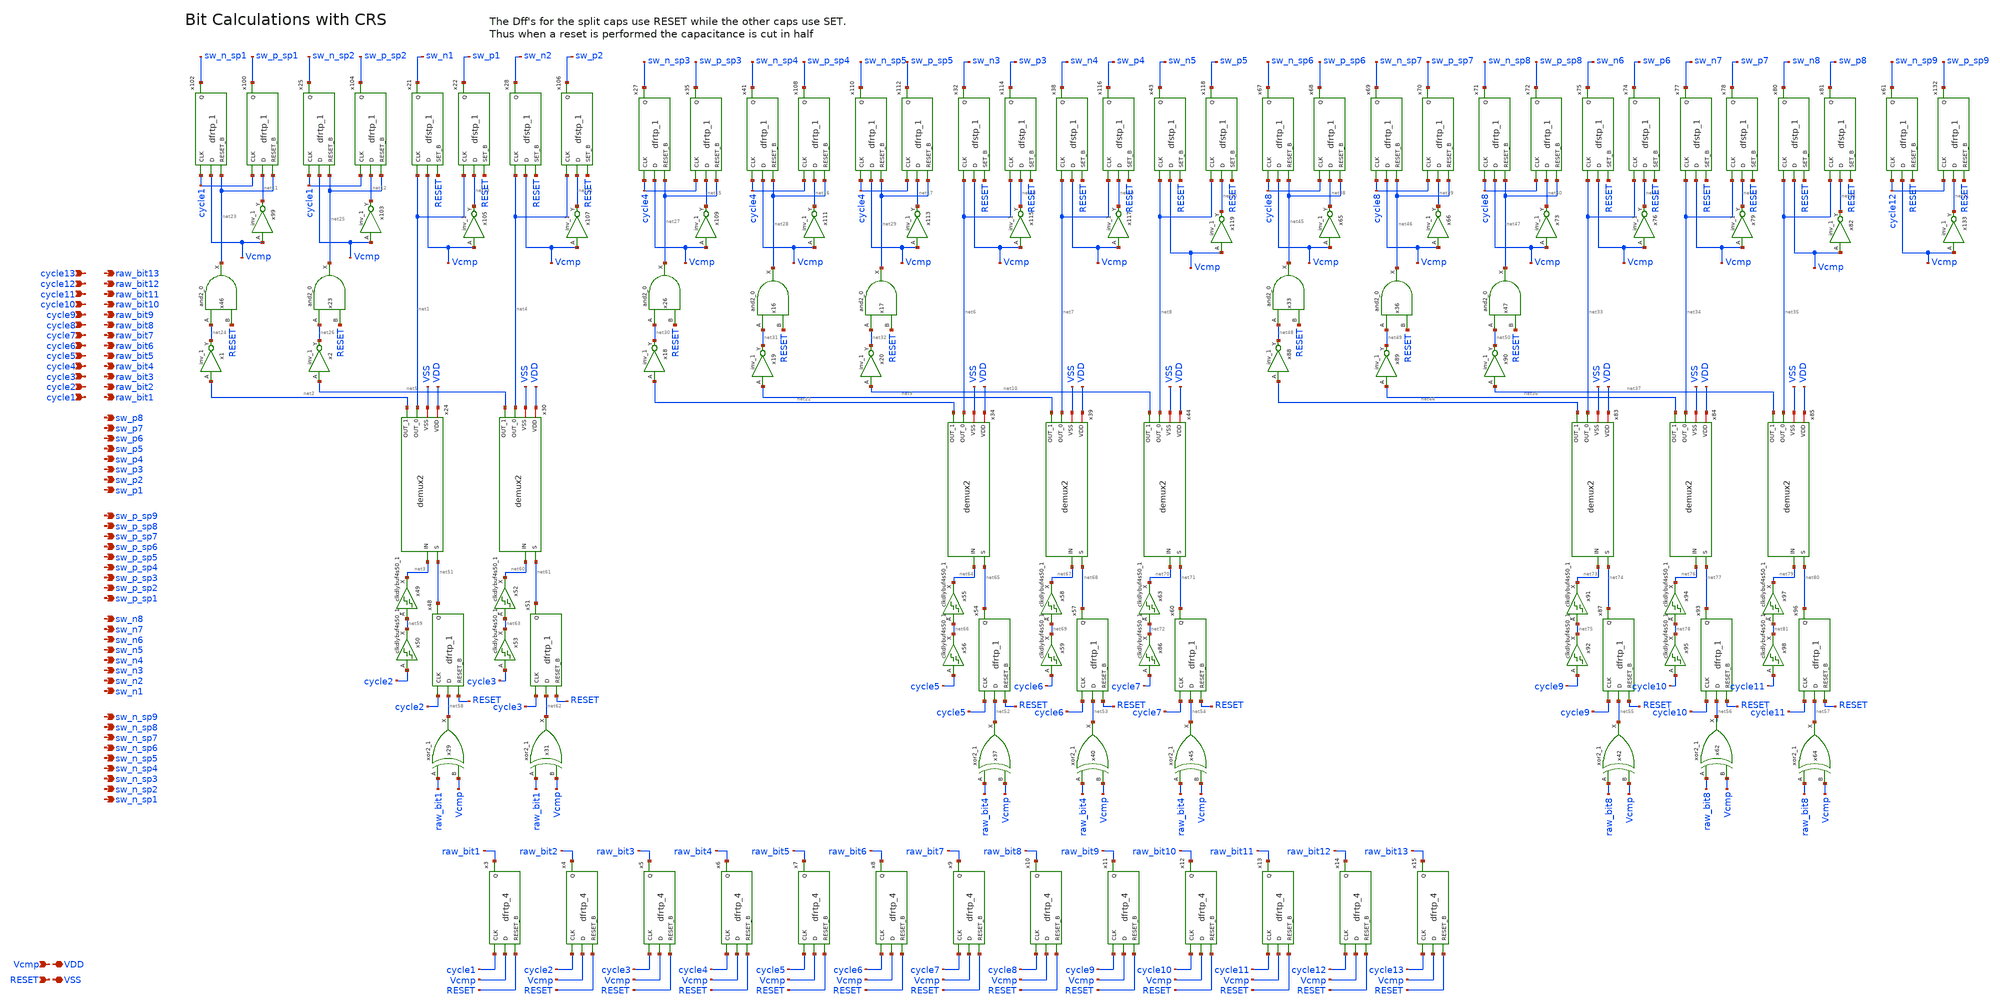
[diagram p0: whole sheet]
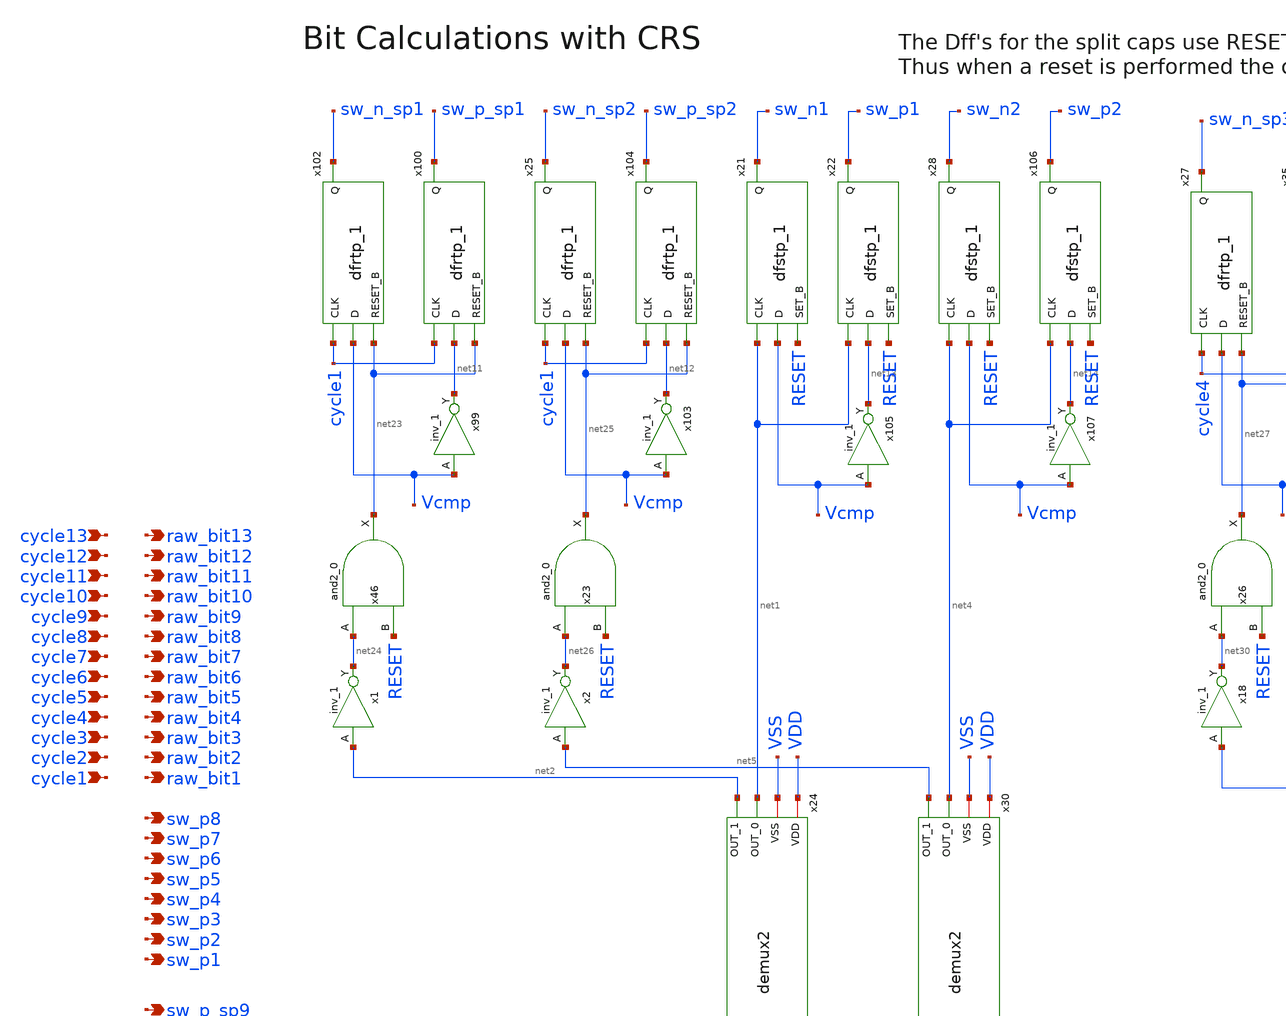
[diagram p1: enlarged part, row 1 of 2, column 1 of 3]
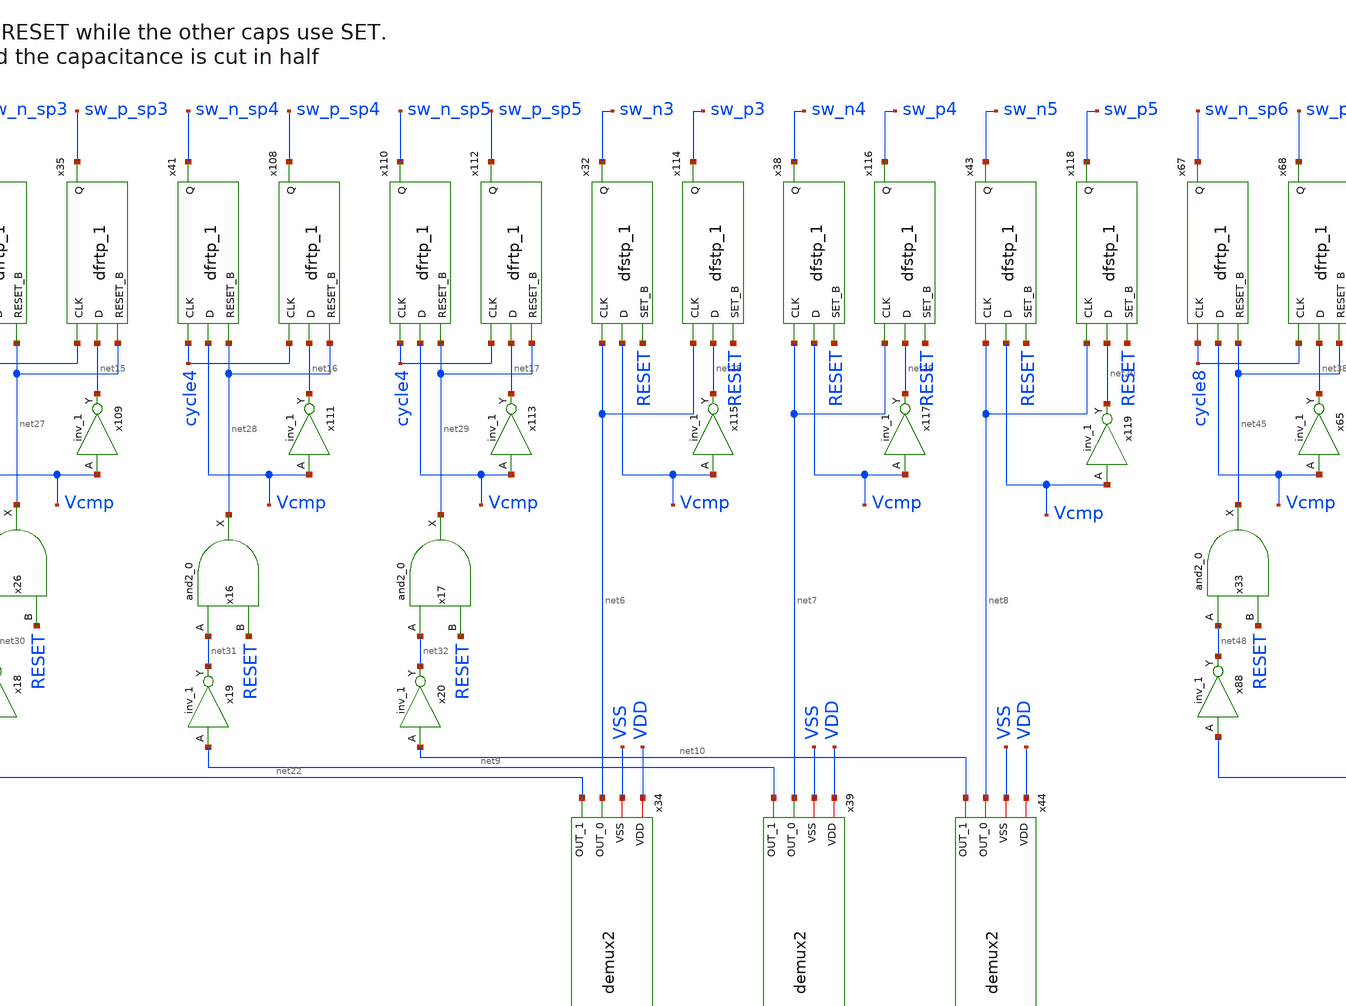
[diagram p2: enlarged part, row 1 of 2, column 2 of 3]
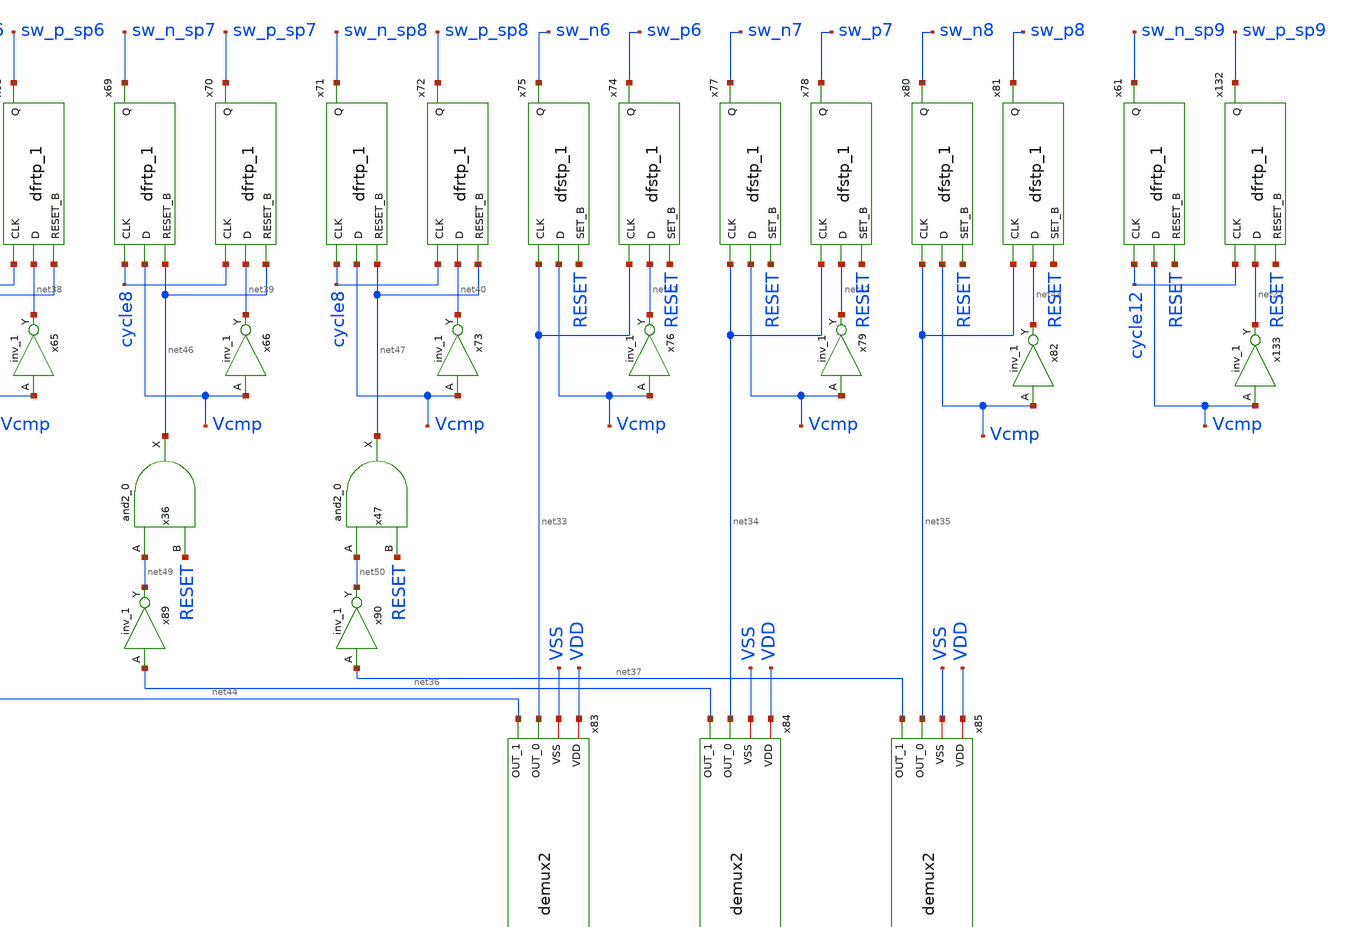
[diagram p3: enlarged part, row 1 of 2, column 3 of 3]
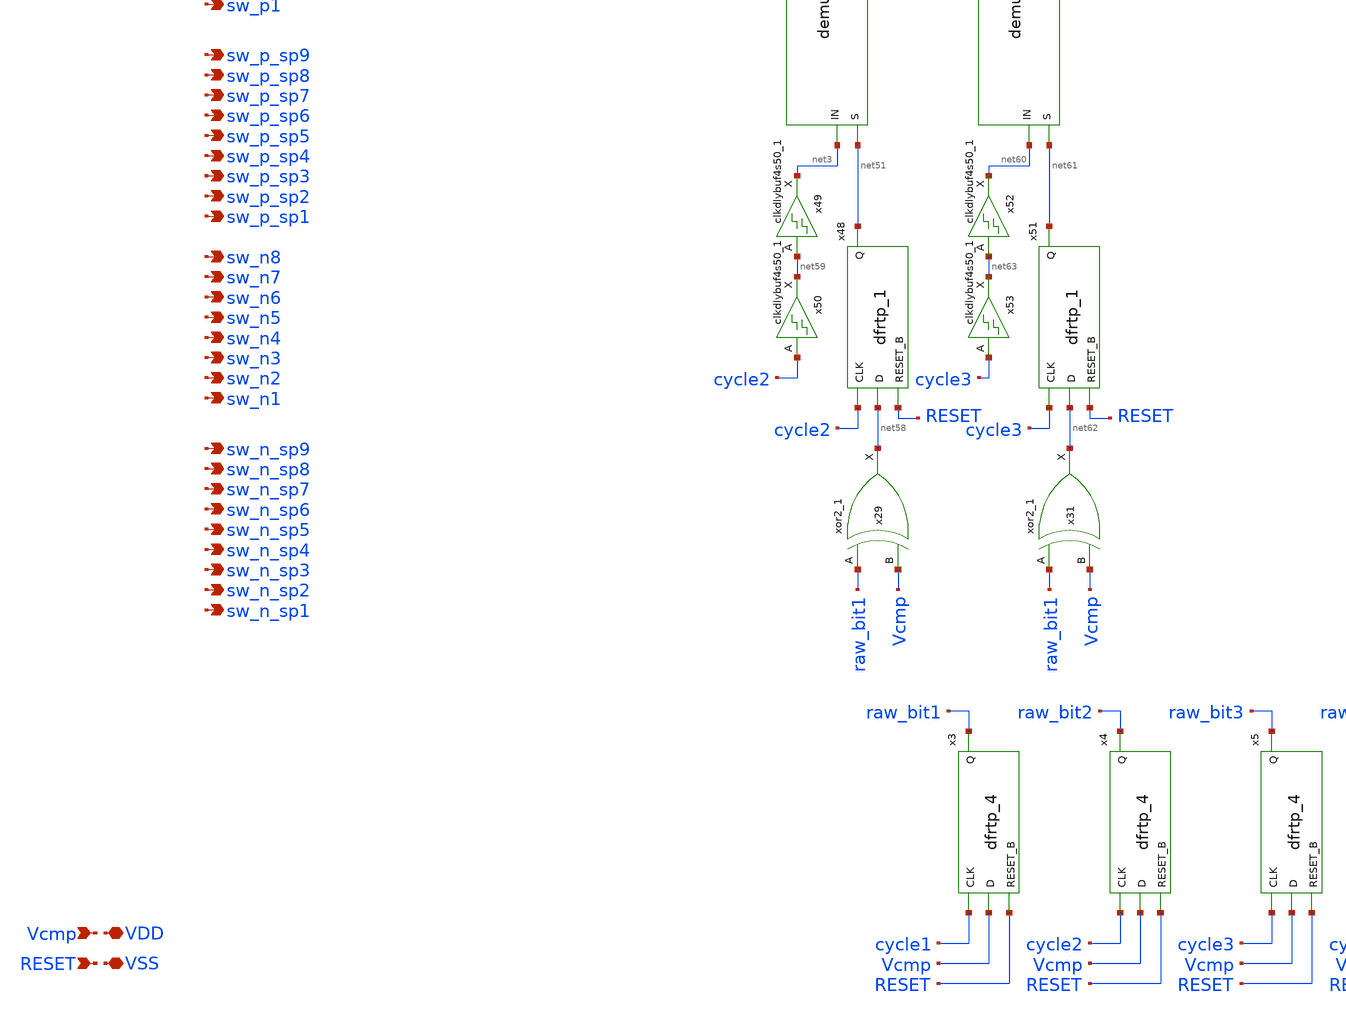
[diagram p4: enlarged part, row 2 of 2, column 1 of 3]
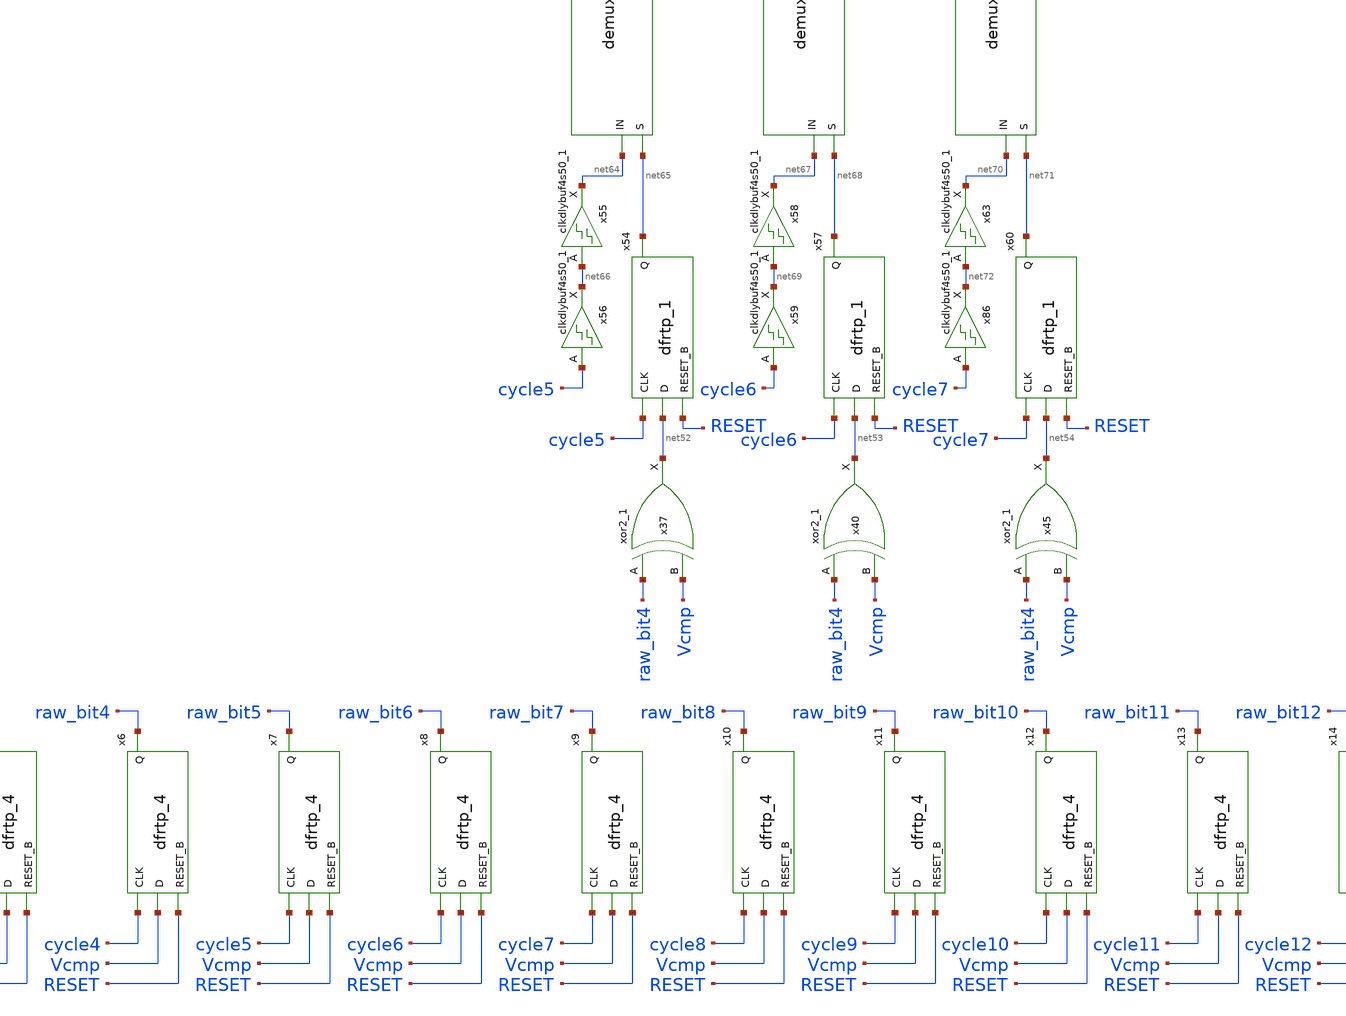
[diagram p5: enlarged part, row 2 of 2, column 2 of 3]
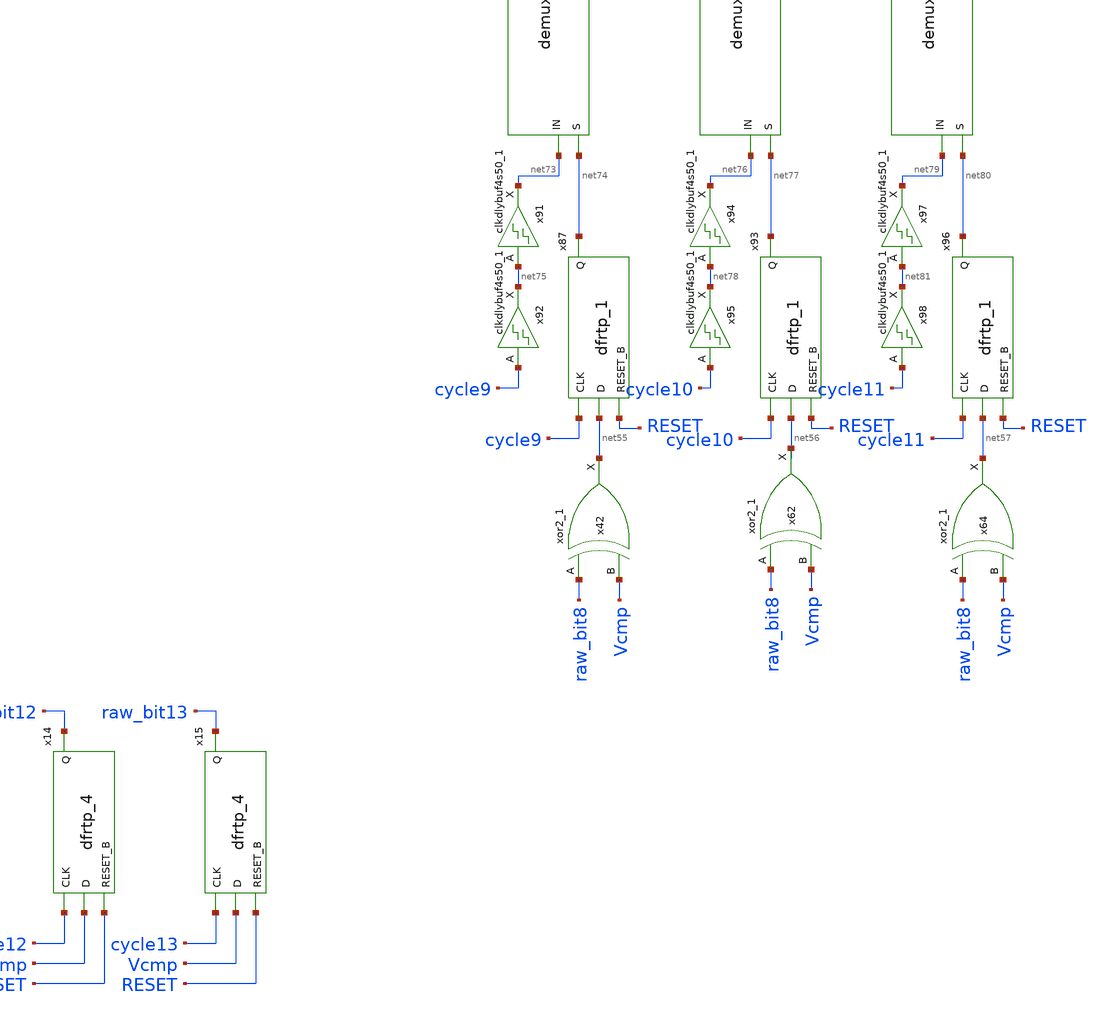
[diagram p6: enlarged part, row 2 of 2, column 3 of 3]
** sch_path: xschem/src/raw_bit_calculator/raw_bit_calculator.sch
**.subckt raw_bit_calculator cycle13 VSS VDD sw_p_sp8 sw_p8 Vcmp RESET raw_bit13 cycle12 cycle11
*+ cycle10 cycle9 cycle8 cycle7 cycle6 cycle5 cycle4 cycle3 cycle2 cycle1 raw_bit12 raw_bit11 raw_bit10
*+ raw_bit9 raw_bit8 raw_bit7 raw_bit6 raw_bit5 raw_bit4 raw_bit3 raw_bit2 raw_bit1 sw_p7 sw_p6 sw_p5 sw_p4
*+ sw_p3 sw_p2 sw_p1 sw_p_sp7 sw_p_sp6 sw_p_sp5 sw_p_sp4 sw_p_sp3 sw_p_sp2 sw_p_sp1 sw_p_sp9 sw_n_sp8 sw_n8
*+ sw_n7 sw_n6 sw_n5 sw_n4 sw_n3 sw_n2 sw_n1 sw_n_sp7 sw_n_sp6 sw_n_sp5 sw_n_sp4 sw_n_sp3 sw_n_sp2 sw_n_sp1
*+ sw_n_sp9
*.ipin cycle13
*.iopin VSS
*.iopin VDD
*.opin sw_p_sp8
*.opin sw_p8
*.ipin Vcmp
*.ipin RESET
*.opin raw_bit13
*.ipin cycle12
*.ipin cycle11
*.ipin cycle10
*.ipin cycle9
*.ipin cycle8
*.ipin cycle7
*.ipin cycle6
*.ipin cycle5
*.ipin cycle4
*.ipin cycle3
*.ipin cycle2
*.ipin cycle1
*.opin raw_bit12
*.opin raw_bit11
*.opin raw_bit10
*.opin raw_bit9
*.opin raw_bit8
*.opin raw_bit7
*.opin raw_bit6
*.opin raw_bit5
*.opin raw_bit4
*.opin raw_bit3
*.opin raw_bit2
*.opin raw_bit1
*.opin sw_p7
*.opin sw_p6
*.opin sw_p5
*.opin sw_p4
*.opin sw_p3
*.opin sw_p2
*.opin sw_p1
*.opin sw_p_sp7
*.opin sw_p_sp6
*.opin sw_p_sp5
*.opin sw_p_sp4
*.opin sw_p_sp3
*.opin sw_p_sp2
*.opin sw_p_sp1
*.opin sw_p_sp9
*.opin sw_n_sp8
*.opin sw_n8
*.opin sw_n7
*.opin sw_n6
*.opin sw_n5
*.opin sw_n4
*.opin sw_n3
*.opin sw_n2
*.opin sw_n1
*.opin sw_n_sp7
*.opin sw_n_sp6
*.opin sw_n_sp5
*.opin sw_n_sp4
*.opin sw_n_sp3
*.opin sw_n_sp2
*.opin sw_n_sp1
*.opin sw_n_sp9
x29 raw_bit1 Vcmp VSS VSS VDD VDD net58 sky130_fd_sc_hd__xor2_1
x31 raw_bit1 Vcmp VSS VSS VDD VDD net62 sky130_fd_sc_hd__xor2_1
x37 raw_bit4 Vcmp VSS VSS VDD VDD net52 sky130_fd_sc_hd__xor2_1
x40 raw_bit4 Vcmp VSS VSS VDD VDD net53 sky130_fd_sc_hd__xor2_1
x45 raw_bit4 Vcmp VSS VSS VDD VDD net54 sky130_fd_sc_hd__xor2_1
x100 cycle1 net11 net23 VSS VSS VDD VDD sw_p_sp1 sky130_fd_sc_hd__dfrtp_1
x99 Vcmp VSS VSS VDD VDD net11 sky130_fd_sc_hd__inv_1
x102 cycle1 Vcmp net23 VSS VSS VDD VDD sw_n_sp1 sky130_fd_sc_hd__dfrtp_1
x25 cycle1 Vcmp net25 VSS VSS VDD VDD sw_n_sp2 sky130_fd_sc_hd__dfrtp_1
x103 Vcmp VSS VSS VDD VDD net12 sky130_fd_sc_hd__inv_1
x104 cycle1 net12 net25 VSS VSS VDD VDD sw_p_sp2 sky130_fd_sc_hd__dfrtp_1
x21 net1 Vcmp RESET VSS VSS VDD VDD sw_n1 sky130_fd_sc_hd__dfstp_1
x22 net1 net13 RESET VSS VSS VDD VDD sw_p1 sky130_fd_sc_hd__dfstp_1
x105 Vcmp VSS VSS VDD VDD net13 sky130_fd_sc_hd__inv_1
x28 net4 Vcmp RESET VSS VSS VDD VDD sw_n2 sky130_fd_sc_hd__dfstp_1
x106 net4 net14 RESET VSS VSS VDD VDD sw_p2 sky130_fd_sc_hd__dfstp_1
x107 Vcmp VSS VSS VDD VDD net14 sky130_fd_sc_hd__inv_1
x109 Vcmp VSS VSS VDD VDD net15 sky130_fd_sc_hd__inv_1
x111 Vcmp VSS VSS VDD VDD net16 sky130_fd_sc_hd__inv_1
x27 cycle4 Vcmp net27 VSS VSS VDD VDD sw_n_sp3 sky130_fd_sc_hd__dfrtp_1
x35 cycle4 net15 net27 VSS VSS VDD VDD sw_p_sp3 sky130_fd_sc_hd__dfrtp_1
x41 cycle4 Vcmp net28 VSS VSS VDD VDD sw_n_sp4 sky130_fd_sc_hd__dfrtp_1
x108 cycle4 net16 net28 VSS VSS VDD VDD sw_p_sp4 sky130_fd_sc_hd__dfrtp_1
x110 cycle4 Vcmp net29 VSS VSS VDD VDD sw_n_sp5 sky130_fd_sc_hd__dfrtp_1
x112 cycle4 net17 net29 VSS VSS VDD VDD sw_p_sp5 sky130_fd_sc_hd__dfrtp_1
x113 Vcmp VSS VSS VDD VDD net17 sky130_fd_sc_hd__inv_1
x114 net6 net18 RESET VSS VSS VDD VDD sw_p3 sky130_fd_sc_hd__dfstp_1
x32 net6 Vcmp RESET VSS VSS VDD VDD sw_n3 sky130_fd_sc_hd__dfstp_1
x115 Vcmp VSS VSS VDD VDD net18 sky130_fd_sc_hd__inv_1
x38 net7 Vcmp RESET VSS VSS VDD VDD sw_n4 sky130_fd_sc_hd__dfstp_1
x116 net7 net19 RESET VSS VSS VDD VDD sw_p4 sky130_fd_sc_hd__dfstp_1
x117 Vcmp VSS VSS VDD VDD net19 sky130_fd_sc_hd__inv_1
x43 net8 Vcmp RESET VSS VSS VDD VDD sw_n5 sky130_fd_sc_hd__dfstp_1
x118 net8 net20 RESET VSS VSS VDD VDD sw_p5 sky130_fd_sc_hd__dfstp_1
x119 Vcmp VSS VSS VDD VDD net20 sky130_fd_sc_hd__inv_1
x132 cycle12 net21 RESET VSS VSS VDD VDD sw_p_sp9 sky130_fd_sc_hd__dfrtp_1
x133 Vcmp VSS VSS VDD VDD net21 sky130_fd_sc_hd__inv_1
x61 cycle12 Vcmp RESET VSS VSS VDD VDD sw_n_sp9 sky130_fd_sc_hd__dfrtp_1
x24 net51 VDD VSS net1 net3 net2 demux2
x30 net61 VDD VSS net4 net60 net5 demux2
x34 net65 VDD VSS net6 net64 net22 demux2
x39 net68 VDD VSS net7 net67 net9 demux2
x44 net71 VDD VSS net8 net70 net10 demux2
x1 net2 VSS VSS VDD VDD net24 sky130_fd_sc_hd__inv_1
x2 net5 VSS VSS VDD VDD net26 sky130_fd_sc_hd__inv_1
x3 cycle1 Vcmp RESET VSS VSS VDD VDD raw_bit1 sky130_fd_sc_hd__dfrtp_4
x4 cycle2 Vcmp RESET VSS VSS VDD VDD raw_bit2 sky130_fd_sc_hd__dfrtp_4
x5 cycle3 Vcmp RESET VSS VSS VDD VDD raw_bit3 sky130_fd_sc_hd__dfrtp_4
x6 cycle4 Vcmp RESET VSS VSS VDD VDD raw_bit4 sky130_fd_sc_hd__dfrtp_4
x7 cycle5 Vcmp RESET VSS VSS VDD VDD raw_bit5 sky130_fd_sc_hd__dfrtp_4
x8 cycle6 Vcmp RESET VSS VSS VDD VDD raw_bit6 sky130_fd_sc_hd__dfrtp_4
x9 cycle7 Vcmp RESET VSS VSS VDD VDD raw_bit7 sky130_fd_sc_hd__dfrtp_4
x10 cycle8 Vcmp RESET VSS VSS VDD VDD raw_bit8 sky130_fd_sc_hd__dfrtp_4
x11 cycle9 Vcmp RESET VSS VSS VDD VDD raw_bit9 sky130_fd_sc_hd__dfrtp_4
x12 cycle10 Vcmp RESET VSS VSS VDD VDD raw_bit10 sky130_fd_sc_hd__dfrtp_4
x13 cycle11 Vcmp RESET VSS VSS VDD VDD raw_bit11 sky130_fd_sc_hd__dfrtp_4
x14 cycle12 Vcmp RESET VSS VSS VDD VDD raw_bit12 sky130_fd_sc_hd__dfrtp_4
x15 cycle13 Vcmp RESET VSS VSS VDD VDD raw_bit13 sky130_fd_sc_hd__dfrtp_4
x18 net22 VSS VSS VDD VDD net30 sky130_fd_sc_hd__inv_1
x19 net9 VSS VSS VDD VDD net31 sky130_fd_sc_hd__inv_1
x20 net10 VSS VSS VDD VDD net32 sky130_fd_sc_hd__inv_1
x42 raw_bit8 Vcmp VSS VSS VDD VDD net55 sky130_fd_sc_hd__xor2_1
x62 raw_bit8 Vcmp VSS VSS VDD VDD net56 sky130_fd_sc_hd__xor2_1
x64 raw_bit8 Vcmp VSS VSS VDD VDD net57 sky130_fd_sc_hd__xor2_1
x65 Vcmp VSS VSS VDD VDD net38 sky130_fd_sc_hd__inv_1
x66 Vcmp VSS VSS VDD VDD net39 sky130_fd_sc_hd__inv_1
x67 cycle8 Vcmp net45 VSS VSS VDD VDD sw_n_sp6 sky130_fd_sc_hd__dfrtp_1
x68 cycle8 net38 net45 VSS VSS VDD VDD sw_p_sp6 sky130_fd_sc_hd__dfrtp_1
x69 cycle8 Vcmp net46 VSS VSS VDD VDD sw_n_sp7 sky130_fd_sc_hd__dfrtp_1
x70 cycle8 net39 net46 VSS VSS VDD VDD sw_p_sp7 sky130_fd_sc_hd__dfrtp_1
x71 cycle8 Vcmp net47 VSS VSS VDD VDD sw_n_sp8 sky130_fd_sc_hd__dfrtp_1
x72 cycle8 net40 net47 VSS VSS VDD VDD sw_p_sp8 sky130_fd_sc_hd__dfrtp_1
x73 Vcmp VSS VSS VDD VDD net40 sky130_fd_sc_hd__inv_1
x74 net33 net41 RESET VSS VSS VDD VDD sw_p6 sky130_fd_sc_hd__dfstp_1
x75 net33 Vcmp RESET VSS VSS VDD VDD sw_n6 sky130_fd_sc_hd__dfstp_1
x76 Vcmp VSS VSS VDD VDD net41 sky130_fd_sc_hd__inv_1
x77 net34 Vcmp RESET VSS VSS VDD VDD sw_n7 sky130_fd_sc_hd__dfstp_1
x78 net34 net42 RESET VSS VSS VDD VDD sw_p7 sky130_fd_sc_hd__dfstp_1
x79 Vcmp VSS VSS VDD VDD net42 sky130_fd_sc_hd__inv_1
x80 net35 Vcmp RESET VSS VSS VDD VDD sw_n8 sky130_fd_sc_hd__dfstp_1
x81 net35 net43 RESET VSS VSS VDD VDD sw_p8 sky130_fd_sc_hd__dfstp_1
x82 Vcmp VSS VSS VDD VDD net43 sky130_fd_sc_hd__inv_1
x83 net74 VDD VSS net33 net73 net44 demux2
x84 net77 VDD VSS net34 net76 net36 demux2
x85 net80 VDD VSS net35 net79 net37 demux2
x88 net44 VSS VSS VDD VDD net48 sky130_fd_sc_hd__inv_1
x89 net36 VSS VSS VDD VDD net49 sky130_fd_sc_hd__inv_1
x90 net37 VSS VSS VDD VDD net50 sky130_fd_sc_hd__inv_1
x46 net24 RESET VSS VSS VDD VDD net23 sky130_fd_sc_hd__and2_0
x23 net26 RESET VSS VSS VDD VDD net25 sky130_fd_sc_hd__and2_0
x26 net30 RESET VSS VSS VDD VDD net27 sky130_fd_sc_hd__and2_0
x16 net31 RESET VSS VSS VDD VDD net28 sky130_fd_sc_hd__and2_0
x17 net32 RESET VSS VSS VDD VDD net29 sky130_fd_sc_hd__and2_0
x33 net48 RESET VSS VSS VDD VDD net45 sky130_fd_sc_hd__and2_0
x36 net49 RESET VSS VSS VDD VDD net46 sky130_fd_sc_hd__and2_0
x47 net50 RESET VSS VSS VDD VDD net47 sky130_fd_sc_hd__and2_0
x48 cycle2 net58 RESET VSS VSS VDD VDD net51 sky130_fd_sc_hd__dfrtp_1
x49 net59 VSS VSS VDD VDD net3 sky130_fd_sc_hd__clkdlybuf4s50_1
x50 cycle2 VSS VSS VDD VDD net59 sky130_fd_sc_hd__clkdlybuf4s50_1
x51 cycle3 net62 RESET VSS VSS VDD VDD net61 sky130_fd_sc_hd__dfrtp_1
x52 net63 VSS VSS VDD VDD net60 sky130_fd_sc_hd__clkdlybuf4s50_1
x53 cycle3 VSS VSS VDD VDD net63 sky130_fd_sc_hd__clkdlybuf4s50_1
x54 cycle5 net52 RESET VSS VSS VDD VDD net65 sky130_fd_sc_hd__dfrtp_1
x55 net66 VSS VSS VDD VDD net64 sky130_fd_sc_hd__clkdlybuf4s50_1
x56 cycle5 VSS VSS VDD VDD net66 sky130_fd_sc_hd__clkdlybuf4s50_1
x57 cycle6 net53 RESET VSS VSS VDD VDD net68 sky130_fd_sc_hd__dfrtp_1
x58 net69 VSS VSS VDD VDD net67 sky130_fd_sc_hd__clkdlybuf4s50_1
x59 cycle6 VSS VSS VDD VDD net69 sky130_fd_sc_hd__clkdlybuf4s50_1
x60 cycle7 net54 RESET VSS VSS VDD VDD net71 sky130_fd_sc_hd__dfrtp_1
x63 net72 VSS VSS VDD VDD net70 sky130_fd_sc_hd__clkdlybuf4s50_1
x86 cycle7 VSS VSS VDD VDD net72 sky130_fd_sc_hd__clkdlybuf4s50_1
x87 cycle9 net55 RESET VSS VSS VDD VDD net74 sky130_fd_sc_hd__dfrtp_1
x91 net75 VSS VSS VDD VDD net73 sky130_fd_sc_hd__clkdlybuf4s50_1
x92 cycle9 VSS VSS VDD VDD net75 sky130_fd_sc_hd__clkdlybuf4s50_1
x93 cycle10 net56 RESET VSS VSS VDD VDD net77 sky130_fd_sc_hd__dfrtp_1
x94 net78 VSS VSS VDD VDD net76 sky130_fd_sc_hd__clkdlybuf4s50_1
x95 cycle10 VSS VSS VDD VDD net78 sky130_fd_sc_hd__clkdlybuf4s50_1
x96 cycle11 net57 RESET VSS VSS VDD VDD net80 sky130_fd_sc_hd__dfrtp_1
x97 net81 VSS VSS VDD VDD net79 sky130_fd_sc_hd__clkdlybuf4s50_1
x98 cycle11 VSS VSS VDD VDD net81 sky130_fd_sc_hd__clkdlybuf4s50_1
**.ends

* expanding   symbol:  src/demux2/demux2.sym # of pins=6
** sym_path: xschem/src/demux2/demux2.sym
** sch_path: xschem/src/demux2/demux2.sch
.subckt demux2 S VDD VSS OUT_0 IN OUT_1
*.ipin S
*.opin OUT_0
*.ipin IN
*.opin OUT_1
*.iopin VDD
*.iopin VSS
x1 net1 IN VSS VSS VDD VDD OUT_0 sky130_fd_sc_hd__and2_0
x2 S IN VSS VSS VDD VDD OUT_1 sky130_fd_sc_hd__and2_0
x3 S VSS VSS VDD VDD net1 sky130_fd_sc_hd__inv_1
.ends

.end
